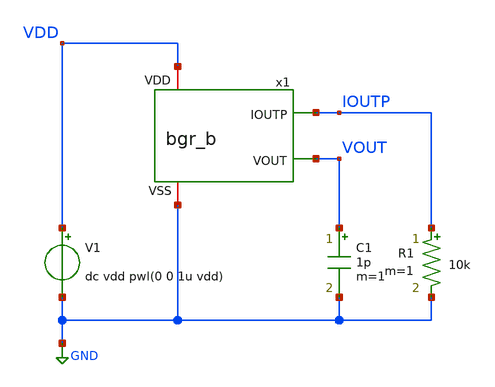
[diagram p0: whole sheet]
** sch_path: member_project/BGR/Maehashi/design/tb_bgr_b.sch
**.subckt tb_bgr_b
x1 VDD IOUTP VOUT GND bgr_b
V1 VDD GND dc vdd pwl(0 0 1u vdd)
C1 VOUT GND 1p m=1
R1 IOUTP GND 10k m=1
**** begin user architecture code


.option savecurrents
.temp 80
.param vthMN = 0.1 ; Slow:0.1, Fast:-0.1
.param vthMP = 0.1 ; Slow:-0.1, Fast:0.1
.param rr = 1      ; Slow:1.15, Fast:0.85
.param vdd = 5
.control
set units=degree
save all

tran 10ns 5us
gnuplot bgrTranStartup_SF v(VDD) v(VOUT)
*plot v(VOUT) ylimit 0 1.2 xlabel Time ylabel Vbgr
*plot @m.x1.xmp3.m1[id] xlabel Temp ylabel Iout

.endc

 .include $::LIB/ip62_models
**** end user architecture code
**.ends
.GLOBAL GND
.end
